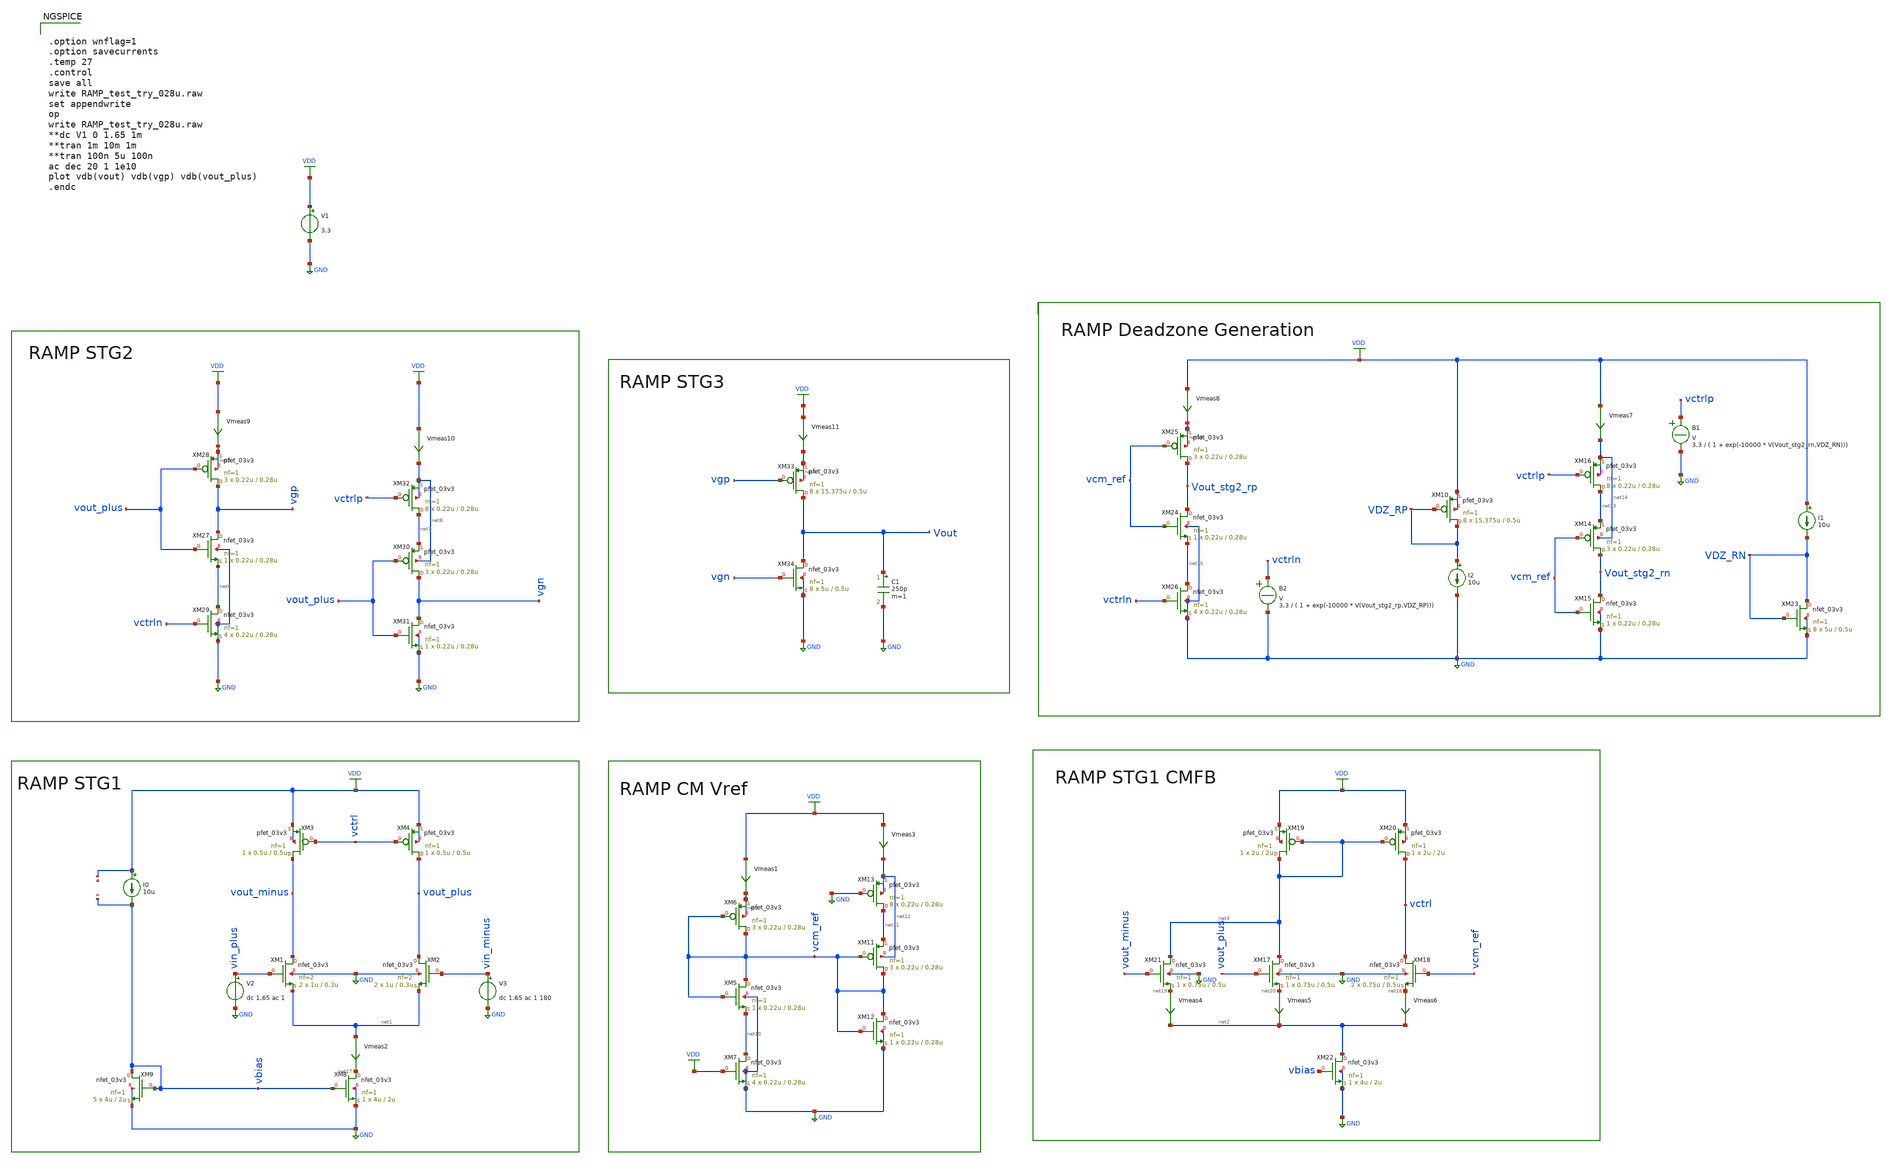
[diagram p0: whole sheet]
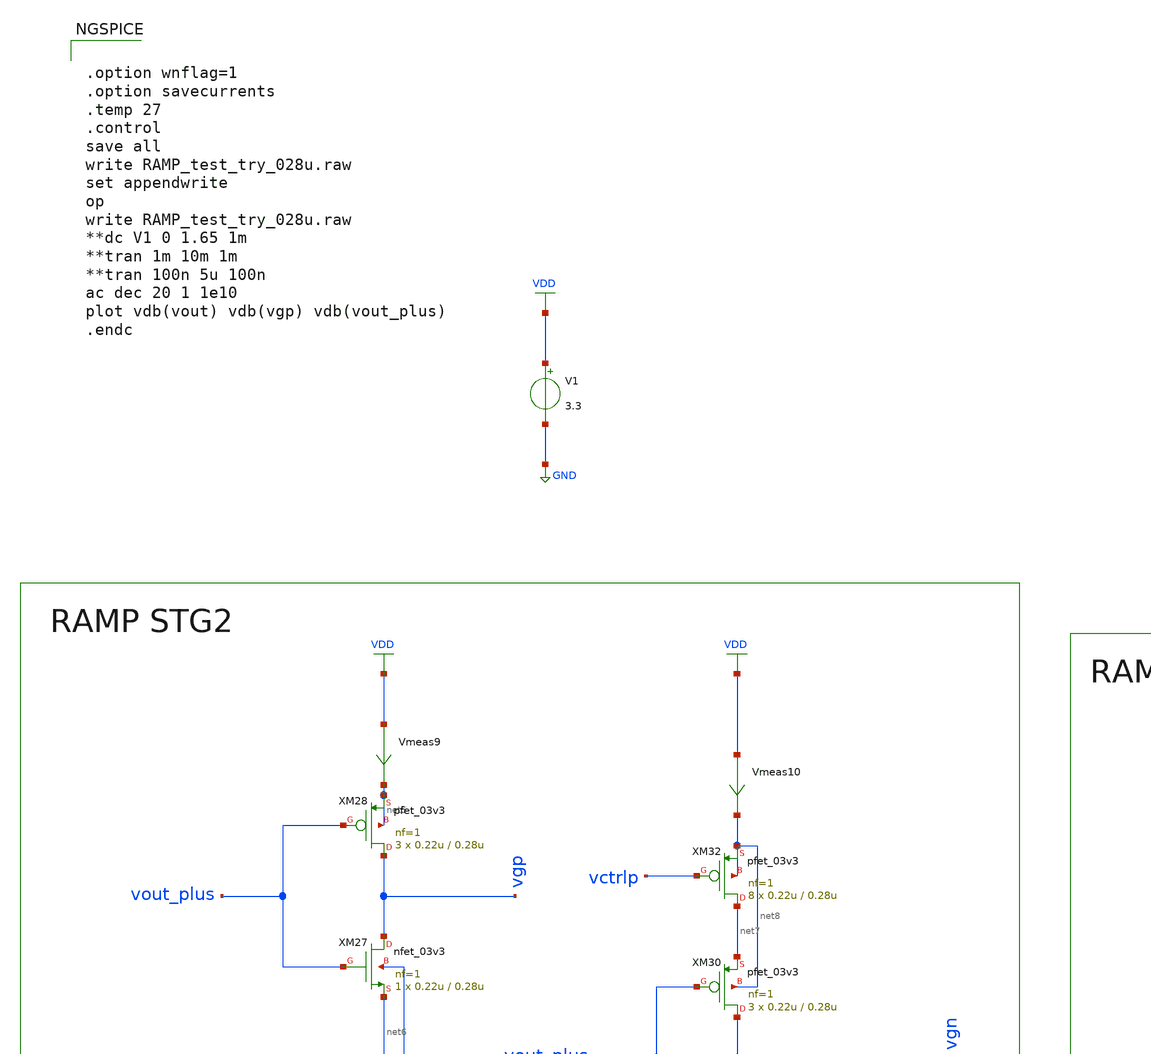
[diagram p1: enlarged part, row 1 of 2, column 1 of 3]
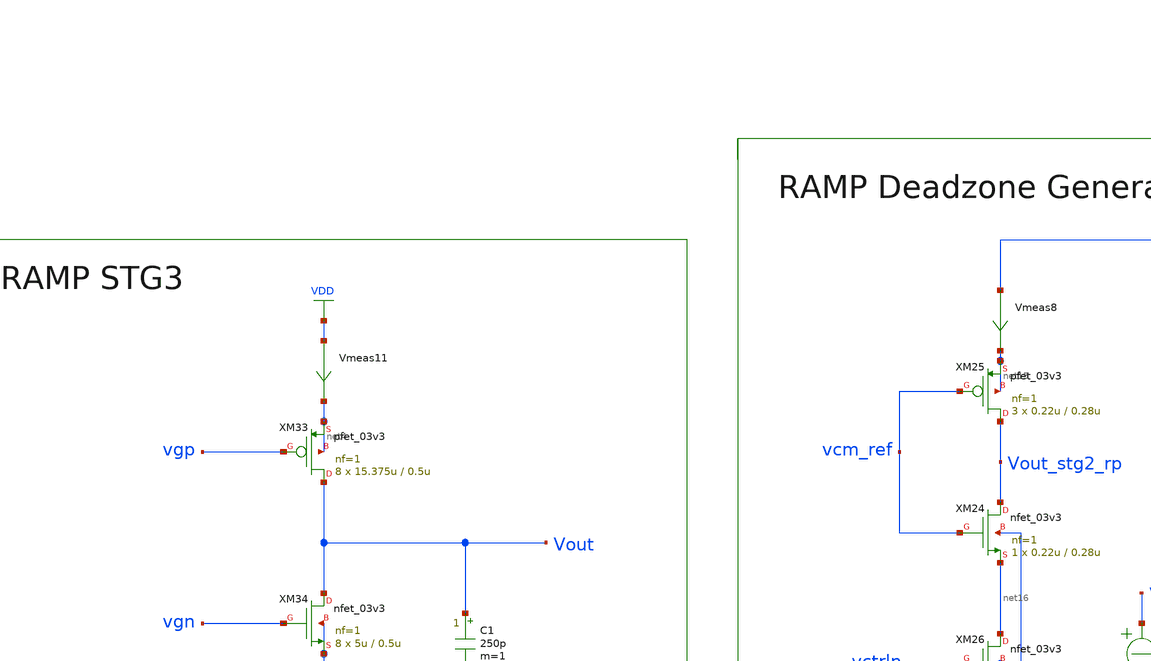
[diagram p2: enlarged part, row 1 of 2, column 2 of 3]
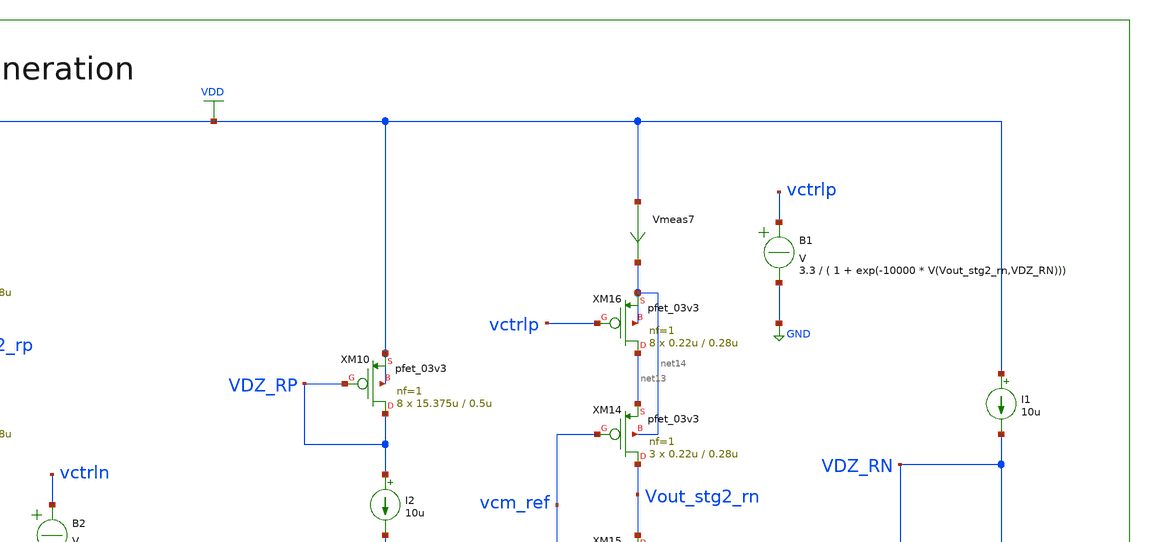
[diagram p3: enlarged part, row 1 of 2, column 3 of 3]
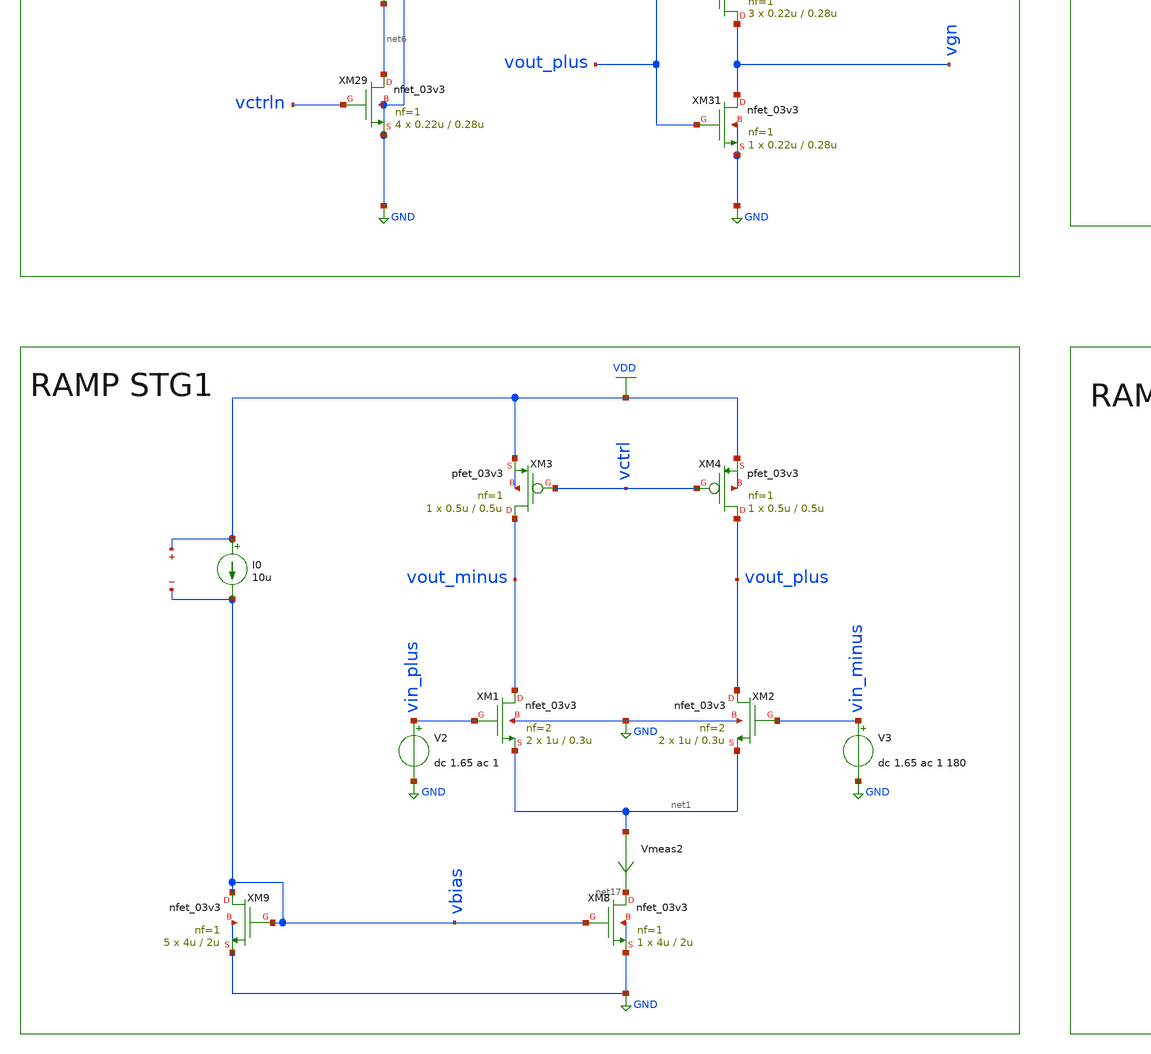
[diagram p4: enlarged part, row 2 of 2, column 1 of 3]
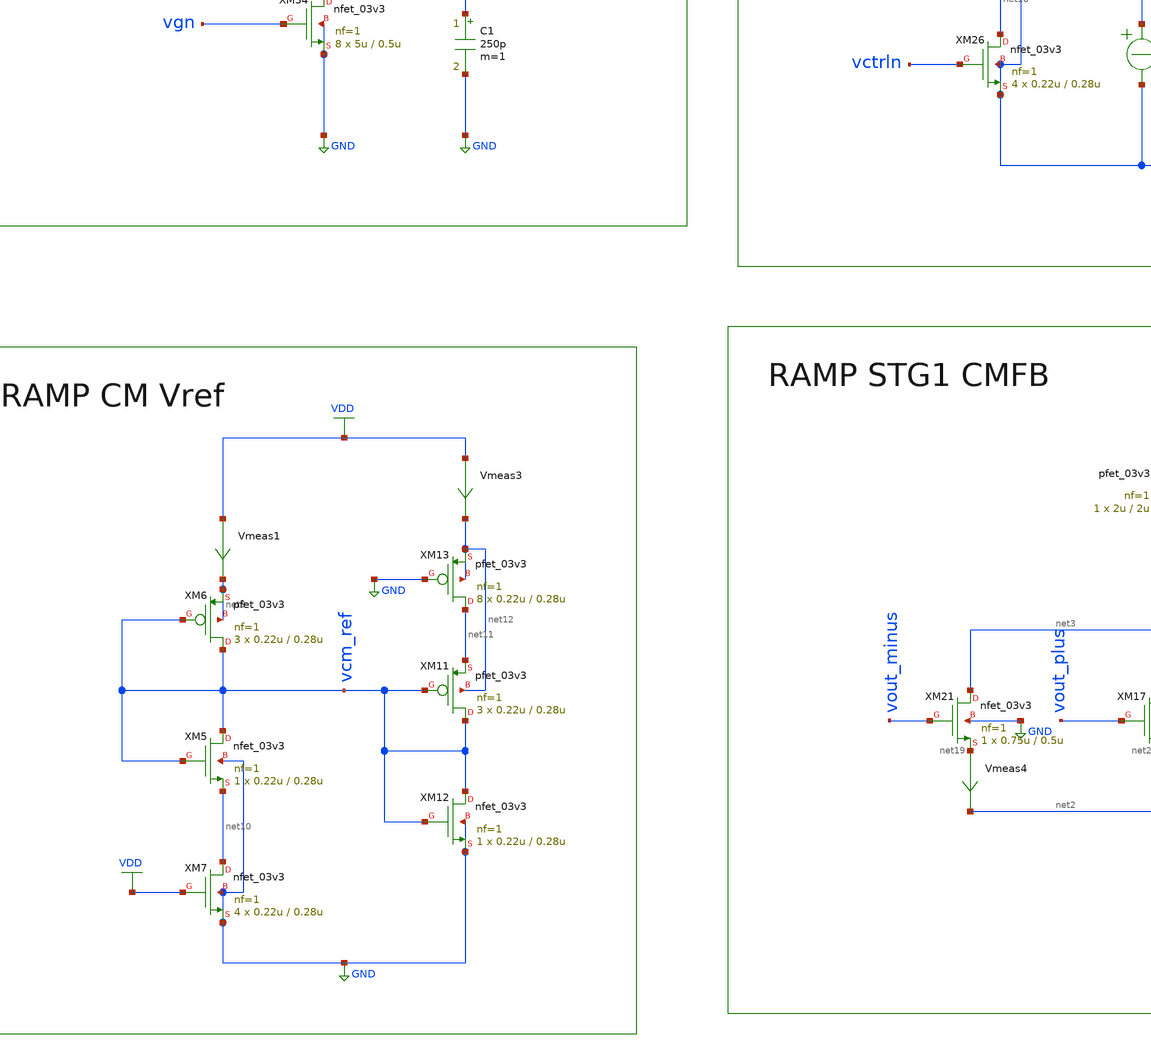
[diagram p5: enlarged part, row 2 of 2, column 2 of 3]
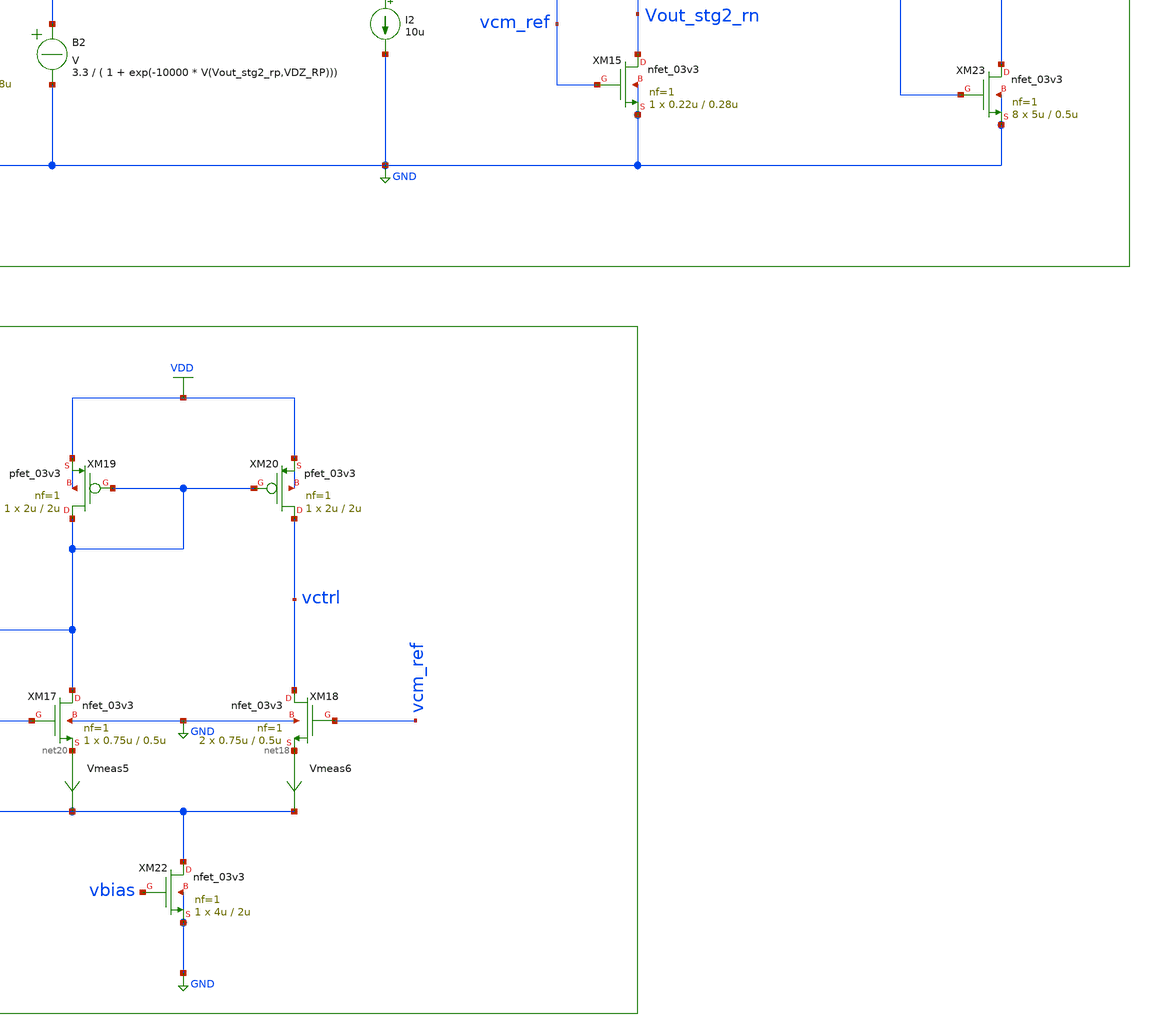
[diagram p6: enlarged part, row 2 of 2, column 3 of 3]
** sch_path: Design_Files/RAMP_test_try_028u.sch
**.subckt RAMP_test_try_028u
XM1 vout_minus vin_plus net1 GND nfet_03v3 L=0.3u W=1u nf=2 ad='int((nf+1)/2) * W/nf * 0.18u' as='int((nf+2)/2) * W/nf * 0.18u'
+ pd='2*int((nf+1)/2) * (W/nf + 0.18u)' ps='2*int((nf+2)/2) * (W/nf + 0.18u)' nrd='0.18u / W' nrs='0.18u / W'
+ sa=0 sb=0 sd=0 m=2
XM3 vout_minus vctrl VDD VDD pfet_03v3 L=0.5u W=0.5u nf=1 ad='int((nf+1)/2) * W/nf * 0.18u' as='int((nf+2)/2) * W/nf * 0.18u'
+ pd='2*int((nf+1)/2) * (W/nf + 0.18u)' ps='2*int((nf+2)/2) * (W/nf + 0.18u)' nrd='0.18u / W' nrs='0.18u / W'
+ sa=0 sb=0 sd=0 m=1
V2 vin_plus GND dc 1.65 ac 1
XM8 net17 vbias GND GND nfet_03v3 L=2u W=4u nf=1 ad='int((nf+1)/2) * W/nf * 0.18u' as='int((nf+2)/2) * W/nf * 0.18u'
+ pd='2*int((nf+1)/2) * (W/nf + 0.18u)' ps='2*int((nf+2)/2) * (W/nf + 0.18u)' nrd='0.18u / W' nrs='0.18u / W'
+ sa=0 sb=0 sd=0 m=1
Vmeas2 net1 net17 0
.save i(vmeas2)
V3 vin_minus GND dc 1.65 ac 1 180
XM9 vbias vbias GND GND nfet_03v3 L=2u W=4u nf=1 ad='int((nf+1)/2) * W/nf * 0.18u' as='int((nf+2)/2) * W/nf * 0.18u'
+ pd='2*int((nf+1)/2) * (W/nf + 0.18u)' ps='2*int((nf+2)/2) * (W/nf + 0.18u)' nrd='0.18u / W' nrs='0.18u / W'
+ sa=0 sb=0 sd=0 m=5
I0 VDD vbias 10u
XM2 vout_plus vin_minus net1 GND nfet_03v3 L=0.3u W=1u nf=2 ad='int((nf+1)/2) * W/nf * 0.18u' as='int((nf+2)/2) * W/nf * 0.18u'
+ pd='2*int((nf+1)/2) * (W/nf + 0.18u)' ps='2*int((nf+2)/2) * (W/nf + 0.18u)' nrd='0.18u / W' nrs='0.18u / W'
+ sa=0 sb=0 sd=0 m=2
XM4 vout_plus vctrl VDD VDD pfet_03v3 L=0.5u W=0.5u nf=1 ad='int((nf+1)/2) * W/nf * 0.18u' as='int((nf+2)/2) * W/nf * 0.18u'
+ pd='2*int((nf+1)/2) * (W/nf + 0.18u)' ps='2*int((nf+2)/2) * (W/nf + 0.18u)' nrd='0.18u / W' nrs='0.18u / W'
+ sa=0 sb=0 sd=0 m=1
V1 VDD GND 3.3
XM18 vctrl vcm_ref net18 GND nfet_03v3 L=0.5u W=0.75u nf=1 ad='int((nf+1)/2) * W/nf * 0.18u' as='int((nf+2)/2) * W/nf * 0.18u'
+ pd='2*int((nf+1)/2) * (W/nf + 0.18u)' ps='2*int((nf+2)/2) * (W/nf + 0.18u)' nrd='0.18u / W' nrs='0.18u / W'
+ sa=0 sb=0 sd=0 m=2
XM19 net3 net3 VDD VDD pfet_03v3 L=2u W=2u nf=1 ad='int((nf+1)/2) * W/nf * 0.18u' as='int((nf+2)/2) * W/nf * 0.18u'
+ pd='2*int((nf+1)/2) * (W/nf + 0.18u)' ps='2*int((nf+2)/2) * (W/nf + 0.18u)' nrd='0.18u / W' nrs='0.18u / W'
+ sa=0 sb=0 sd=0 m=1
XM20 vctrl net3 VDD VDD pfet_03v3 L=2u W=2u nf=1 ad='int((nf+1)/2) * W/nf * 0.18u' as='int((nf+2)/2) * W/nf * 0.18u'
+ pd='2*int((nf+1)/2) * (W/nf + 0.18u)' ps='2*int((nf+2)/2) * (W/nf + 0.18u)' nrd='0.18u / W' nrs='0.18u / W'
+ sa=0 sb=0 sd=0 m=1
XM21 net3 vout_minus net19 GND nfet_03v3 L=0.5u W=0.75u nf=1 ad='int((nf+1)/2) * W/nf * 0.18u' as='int((nf+2)/2) * W/nf * 0.18u'
+ pd='2*int((nf+1)/2) * (W/nf + 0.18u)' ps='2*int((nf+2)/2) * (W/nf + 0.18u)' nrd='0.18u / W' nrs='0.18u / W'
+ sa=0 sb=0 sd=0 m=1
XM22 net2 vbias GND GND nfet_03v3 L=2u W=4u nf=1 ad='int((nf+1)/2) * W/nf * 0.18u' as='int((nf+2)/2) * W/nf * 0.18u'
+ pd='2*int((nf+1)/2) * (W/nf + 0.18u)' ps='2*int((nf+2)/2) * (W/nf + 0.18u)' nrd='0.18u / W' nrs='0.18u / W'
+ sa=0 sb=0 sd=0 m=1
XM17 net3 vout_plus net20 GND nfet_03v3 L=0.5u W=0.75u nf=1 ad='int((nf+1)/2) * W/nf * 0.18u' as='int((nf+2)/2) * W/nf * 0.18u'
+ pd='2*int((nf+1)/2) * (W/nf + 0.18u)' ps='2*int((nf+2)/2) * (W/nf + 0.18u)' nrd='0.18u / W' nrs='0.18u / W'
+ sa=0 sb=0 sd=0 m=1
Vmeas4 net19 net2 0
.save i(vmeas4)
Vmeas5 net20 net2 0
.save i(vmeas5)
Vmeas6 net18 net2 0
.save i(vmeas6)
XM33 Vout vgp net4 net4 pfet_03v3 L=0.5u W=15.375u nf=1 ad='int((nf+1)/2) * W/nf * 0.18u' as='int((nf+2)/2) * W/nf * 0.18u'
+ pd='2*int((nf+1)/2) * (W/nf + 0.18u)' ps='2*int((nf+2)/2) * (W/nf + 0.18u)' nrd='0.18u / W' nrs='0.18u / W'
+ sa=0 sb=0 sd=0 m=8
XM34 Vout vgn GND GND nfet_03v3 L=0.5u W=5u nf=1 ad='int((nf+1)/2) * W/nf * 0.18u' as='int((nf+2)/2) * W/nf * 0.18u'
+ pd='2*int((nf+1)/2) * (W/nf + 0.18u)' ps='2*int((nf+2)/2) * (W/nf + 0.18u)' nrd='0.18u / W' nrs='0.18u / W'
+ sa=0 sb=0 sd=0 m=8
C1 Vout GND 250p m=1
XM27 vgp vout_plus net6 GND nfet_03v3 L=0.28u W=0.22u nf=1 ad='int((nf+1)/2) * W/nf * 0.18u' as='int((nf+2)/2) * W/nf * 0.18u'
+ pd='2*int((nf+1)/2) * (W/nf + 0.18u)' ps='2*int((nf+2)/2) * (W/nf + 0.18u)' nrd='0.18u / W' nrs='0.18u / W'
+ sa=0 sb=0 sd=0 m=1
XM28 vgp vout_plus net5 net5 pfet_03v3 L=0.28u W=0.22u nf=1 ad='int((nf+1)/2) * W/nf * 0.18u' as='int((nf+2)/2) * W/nf * 0.18u'
+ pd='2*int((nf+1)/2) * (W/nf + 0.18u)' ps='2*int((nf+2)/2) * (W/nf + 0.18u)' nrd='0.18u / W' nrs='0.18u / W'
+ sa=0 sb=0 sd=0 m=3
XM29 net6 vctrln GND GND nfet_03v3 L=0.28u W=0.22u nf=1 ad='int((nf+1)/2) * W/nf * 0.18u' as='int((nf+2)/2) * W/nf * 0.18u'
+ pd='2*int((nf+1)/2) * (W/nf + 0.18u)' ps='2*int((nf+2)/2) * (W/nf + 0.18u)' nrd='0.18u / W' nrs='0.18u / W'
+ sa=0 sb=0 sd=0 m=4
Vmeas9 VDD net5 0
.save i(vmeas9)
XM30 vgn vout_plus net7 net8 pfet_03v3 L=0.28u W=0.22u nf=1 ad='int((nf+1)/2) * W/nf * 0.18u' as='int((nf+2)/2) * W/nf * 0.18u'
+ pd='2*int((nf+1)/2) * (W/nf + 0.18u)' ps='2*int((nf+2)/2) * (W/nf + 0.18u)' nrd='0.18u / W' nrs='0.18u / W'
+ sa=0 sb=0 sd=0 m=3
XM31 vgn vout_plus GND GND nfet_03v3 L=0.28u W=0.22u nf=1 ad='int((nf+1)/2) * W/nf * 0.18u' as='int((nf+2)/2) * W/nf * 0.18u'
+ pd='2*int((nf+1)/2) * (W/nf + 0.18u)' ps='2*int((nf+2)/2) * (W/nf + 0.18u)' nrd='0.18u / W' nrs='0.18u / W'
+ sa=0 sb=0 sd=0 m=1
XM32 net7 vctrlp net8 net8 pfet_03v3 L=0.28u W=0.22u nf=1 ad='int((nf+1)/2) * W/nf * 0.18u' as='int((nf+2)/2) * W/nf * 0.18u'
+ pd='2*int((nf+1)/2) * (W/nf + 0.18u)' ps='2*int((nf+2)/2) * (W/nf + 0.18u)' nrd='0.18u / W' nrs='0.18u / W'
+ sa=0 sb=0 sd=0 m=8
Vmeas10 VDD net8 0
.save i(vmeas10)
XM5 vcm_ref vcm_ref net10 GND nfet_03v3 L=0.28u W=0.22u nf=1 ad='int((nf+1)/2) * W/nf * 0.18u' as='int((nf+2)/2) * W/nf * 0.18u'
+ pd='2*int((nf+1)/2) * (W/nf + 0.18u)' ps='2*int((nf+2)/2) * (W/nf + 0.18u)' nrd='0.18u / W' nrs='0.18u / W'
+ sa=0 sb=0 sd=0 m=1
XM6 vcm_ref vcm_ref net9 net9 pfet_03v3 L=0.28u W=0.22u nf=1 ad='int((nf+1)/2) * W/nf * 0.18u' as='int((nf+2)/2) * W/nf * 0.18u'
+ pd='2*int((nf+1)/2) * (W/nf + 0.18u)' ps='2*int((nf+2)/2) * (W/nf + 0.18u)' nrd='0.18u / W' nrs='0.18u / W'
+ sa=0 sb=0 sd=0 m=3
XM7 net10 VDD GND GND nfet_03v3 L=0.28u W=0.22u nf=1 ad='int((nf+1)/2) * W/nf * 0.18u' as='int((nf+2)/2) * W/nf * 0.18u'
+ pd='2*int((nf+1)/2) * (W/nf + 0.18u)' ps='2*int((nf+2)/2) * (W/nf + 0.18u)' nrd='0.18u / W' nrs='0.18u / W'
+ sa=0 sb=0 sd=0 m=4
Vmeas1 VDD net9 0
.save i(vmeas1)
XM11 vcm_ref vcm_ref net11 net12 pfet_03v3 L=0.28u W=0.22u nf=1 ad='int((nf+1)/2) * W/nf * 0.18u' as='int((nf+2)/2) * W/nf * 0.18u'
+ pd='2*int((nf+1)/2) * (W/nf + 0.18u)' ps='2*int((nf+2)/2) * (W/nf + 0.18u)' nrd='0.18u / W' nrs='0.18u / W'
+ sa=0 sb=0 sd=0 m=3
XM12 vcm_ref vcm_ref GND GND nfet_03v3 L=0.28u W=0.22u nf=1 ad='int((nf+1)/2) * W/nf * 0.18u' as='int((nf+2)/2) * W/nf * 0.18u'
+ pd='2*int((nf+1)/2) * (W/nf + 0.18u)' ps='2*int((nf+2)/2) * (W/nf + 0.18u)' nrd='0.18u / W' nrs='0.18u / W'
+ sa=0 sb=0 sd=0 m=1
XM13 net11 GND net12 net12 pfet_03v3 L=0.28u W=0.22u nf=1 ad='int((nf+1)/2) * W/nf * 0.18u' as='int((nf+2)/2) * W/nf * 0.18u'
+ pd='2*int((nf+1)/2) * (W/nf + 0.18u)' ps='2*int((nf+2)/2) * (W/nf + 0.18u)' nrd='0.18u / W' nrs='0.18u / W'
+ sa=0 sb=0 sd=0 m=8
Vmeas3 VDD net12 0
.save i(vmeas3)
XM10 VDZ_RP VDZ_RP VDD VDD pfet_03v3 L=0.5u W=15.375u nf=1 ad='int((nf+1)/2) * W/nf * 0.18u' as='int((nf+2)/2) * W/nf * 0.18u'
+ pd='2*int((nf+1)/2) * (W/nf + 0.18u)' ps='2*int((nf+2)/2) * (W/nf + 0.18u)' nrd='0.18u / W' nrs='0.18u / W'
+ sa=0 sb=0 sd=0 m=8
I2 VDZ_RP GND 10u
B2 vctrln GND V = 3.3 / ( 1 + exp(-10000 * V(Vout_stg2_rp,VDZ_RP)))
XM14 Vout_stg2_rn vcm_ref net13 net14 pfet_03v3 L=0.28u W=0.22u nf=1 ad='int((nf+1)/2) * W/nf * 0.18u'
+ as='int((nf+2)/2) * W/nf * 0.18u' pd='2*int((nf+1)/2) * (W/nf + 0.18u)' ps='2*int((nf+2)/2) * (W/nf + 0.18u)'
+ nrd='0.18u / W' nrs='0.18u / W' sa=0 sb=0 sd=0 m=3
XM15 Vout_stg2_rn vcm_ref GND GND nfet_03v3 L=0.28u W=0.22u nf=1 ad='int((nf+1)/2) * W/nf * 0.18u' as='int((nf+2)/2) * W/nf * 0.18u'
+ pd='2*int((nf+1)/2) * (W/nf + 0.18u)' ps='2*int((nf+2)/2) * (W/nf + 0.18u)' nrd='0.18u / W' nrs='0.18u / W'
+ sa=0 sb=0 sd=0 m=1
XM16 net13 vctrlp net14 net14 pfet_03v3 L=0.28u W=0.22u nf=1 ad='int((nf+1)/2) * W/nf * 0.18u' as='int((nf+2)/2) * W/nf * 0.18u'
+ pd='2*int((nf+1)/2) * (W/nf + 0.18u)' ps='2*int((nf+2)/2) * (W/nf + 0.18u)' nrd='0.18u / W' nrs='0.18u / W'
+ sa=0 sb=0 sd=0 m=8
Vmeas7 VDD net14 0
.save i(vmeas7)
XM23 VDZ_RN VDZ_RN GND GND nfet_03v3 L=0.5u W=5u nf=1 ad='int((nf+1)/2) * W/nf * 0.18u' as='int((nf+2)/2) * W/nf * 0.18u'
+ pd='2*int((nf+1)/2) * (W/nf + 0.18u)' ps='2*int((nf+2)/2) * (W/nf + 0.18u)' nrd='0.18u / W' nrs='0.18u / W'
+ sa=0 sb=0 sd=0 m=8
I1 VDD VDZ_RN 10u
B1 vctrlp GND V = 3.3 / ( 1 + exp(-10000 * V(Vout_stg2_rn,VDZ_RN)))
XM24 Vout_stg2_rp vcm_ref net16 GND nfet_03v3 L=0.28u W=0.22u nf=1 ad='int((nf+1)/2) * W/nf * 0.18u'
+ as='int((nf+2)/2) * W/nf * 0.18u' pd='2*int((nf+1)/2) * (W/nf + 0.18u)' ps='2*int((nf+2)/2) * (W/nf + 0.18u)'
+ nrd='0.18u / W' nrs='0.18u / W' sa=0 sb=0 sd=0 m=1
XM25 Vout_stg2_rp vcm_ref net15 net15 pfet_03v3 L=0.28u W=0.22u nf=1 ad='int((nf+1)/2) * W/nf * 0.18u'
+ as='int((nf+2)/2) * W/nf * 0.18u' pd='2*int((nf+1)/2) * (W/nf + 0.18u)' ps='2*int((nf+2)/2) * (W/nf + 0.18u)'
+ nrd='0.18u / W' nrs='0.18u / W' sa=0 sb=0 sd=0 m=3
XM26 net16 vctrln GND GND nfet_03v3 L=0.28u W=0.22u nf=1 ad='int((nf+1)/2) * W/nf * 0.18u' as='int((nf+2)/2) * W/nf * 0.18u'
+ pd='2*int((nf+1)/2) * (W/nf + 0.18u)' ps='2*int((nf+2)/2) * (W/nf + 0.18u)' nrd='0.18u / W' nrs='0.18u / W'
+ sa=0 sb=0 sd=0 m=4
Vmeas8 VDD net15 0
.save i(vmeas8)
Vmeas11 VDD net4 0
.save i(vmeas11)
.save v(vdd)
.save v(vbias)
**** begin user architecture code


.option wnflag=1
.option savecurrents
.temp 27
.control
save all
write RAMP_test_try_028u.raw
set appendwrite
op
write RAMP_test_try_028u.raw
**dc V1 0 1.65 1m
**tran 1m 10m 1m
**tran 100n 5u 100n
ac dec 20 1 1e10
plot vdb(vout) vdb(vgp) vdb(vout_plus)
.endc




 .save @m.xm1.m0[gm]
.save @m.xm1.m0[id]
.save @m.xm1.m0[vth]
.save @m.xm1.m0[vds]
.save @m.xm1.m0[gds]
.save @m.xm1.m0[cgg]
.save @m.xm1.m0[cgs]
.save @m.xm1.m0[cgd]
.save @m.xm2.m0[gm]
.save @m.xm2.m0[id]
.save @m.xm2.m0[vth]
.save @m.xm2.m0[vds]
.save @m.xm2.m0[gds]
.save @m.xm2.m0[cgg]
.save @m.xm2.m0[cgs]
.save @m.xm2.m0[cgd]
.save @m.xm3.m0[gm]
.save @m.xm3.m0[id]
.save @m.xm3.m0[vth]
.save @m.xm3.m0[vds]
.save @m.xm3.m0[gds]
.save @m.xm3.m0[cgg]
.save @m.xm3.m0[cgs]
.save @m.xm3.m0[cgd]
.save @m.xm4.m0[gm]
.save @m.xm4.m0[id]
.save @m.xm4.m0[vth]
.save @m.xm4.m0[vds]
.save @m.xm4.m0[gds]
.save @m.xm4.m0[cgg]
.save @m.xm4.m0[cgs]
.save @m.xm4.m0[cgd]
.save @m.xm5.m0[gm]
.save @m.xm5.m0[id]
.save @m.xm5.m0[vth]
.save @m.xm5.m0[vds]
.save @m.xm5.m0[gds]
.save @m.xm5.m0[cgg]
.save @m.xm5.m0[cgs]
.save @m.xm5.m0[cgd]
.save @m.xm6.m0[gm]
.save @m.xm6.m0[id]
.save @m.xm6.m0[vth]
.save @m.xm6.m0[vds]
.save @m.xm6.m0[gds]
.save @m.xm6.m0[cgg]
.save @m.xm6.m0[cgs]
.save @m.xm6.m0[cgd]
.save @m.xm7.m0[gm]
.save @m.xm7.m0[id]
.save @m.xm7.m0[vth]
.save @m.xm7.m0[vds]
.save @m.xm7.m0[gds]
.save @m.xm7.m0[cgg]
.save @m.xm7.m0[cgs]
.save @m.xm7.m0[cgd]
.save @m.xm8.m0[gm]
.save @m.xm8.m0[id]
.save @m.xm8.m0[vth]
.save @m.xm8.m0[vds]
.save @m.xm8.m0[gds]
.save @m.xm8.m0[cgg]
.save @m.xm8.m0[cgs]
.save @m.xm8.m0[cgd]
.save @m.xm9.m0[gm]
.save @m.xm9.m0[id]
.save @m.xm9.m0[vth]
.save @m.xm9.m0[vds]
.save @m.xm9.m0[gds]
.save @m.xm9.m0[cgg]
.save @m.xm9.m0[cgs]
.save @m.xm9.m0[cgd]
.save @m.xm10.m0[gm]
.save @m.xm10.m0[id]
.save @m.xm10.m0[vth]
.save @m.xm10.m0[vds]
.save @m.xm10.m0[gds]
.save @m.xm10.m0[cgg]
.save @m.xm10.m0[cgs]
.save @m.xm10.m0[cgd]
.save @m.xm11.m0[gm]
.save @m.xm11.m0[id]
.save @m.xm11.m0[vth]
.save @m.xm11.m0[vds]
.save @m.xm11.m0[gds]
.save @m.xm11.m0[cgg]
.save @m.xm11.m0[cgs]
.save @m.xm11.m0[cgd]
.save @m.xm12.m0[gm]
.save @m.xm12.m0[id]
.save @m.xm12.m0[vth]
.save @m.xm12.m0[vds]
.save @m.xm12.m0[gds]
.save @m.xm12.m0[cgg]
.save @m.xm12.m0[cgs]
.save @m.xm12.m0[cgd]
.save @m.xm13.m0[gm]
.save @m.xm13.m0[id]
.save @m.xm13.m0[vth]
.save @m.xm13.m0[vds]
.save @m.xm13.m0[gds]
.save @m.xm13.m0[cgg]
.save @m.xm13.m0[cgs]
.save @m.xm13.m0[cgd]
.save @m.xm14.m0[gm]
.save @m.xm14.m0[id]
.save @m.xm14.m0[vth]
.save @m.xm14.m0[vds]
.save @m.xm14.m0[gds]
.save @m.xm14.m0[cgg]
.save @m.xm14.m0[cgs]
.save @m.xm14.m0[cgd]
.save @m.xm15.m0[gm]
.save @m.xm15.m0[id]
.save @m.xm15.m0[vth]
.save @m.xm15.m0[vds]
.save @m.xm15.m0[gds]
.save @m.xm15.m0[cgg]
.save @m.xm15.m0[cgs]
.save @m.xm15.m0[cgd]
.save @m.xm16.m0[gm]
.save @m.xm16.m0[id]
.save @m.xm16.m0[vth]
.save @m.xm16.m0[vds]
.save @m.xm16.m0[gds]
.save @m.xm16.m0[cgg]
.save @m.xm16.m0[cgs]
.save @m.xm16.m0[cgd]
.save @m.xm17.m0[gm]
.save @m.xm17.m0[id]
.save @m.xm17.m0[vth]
.save @m.xm17.m0[vds]
.save @m.xm17.m0[gds]
.save @m.xm17.m0[cgg]
.save @m.xm17.m0[cgs]
.save @m.xm17.m0[cgd]
.save @m.xm18.m0[gm]
.save @m.xm18.m0[id]
.save @m.xm18.m0[vth]
.save @m.xm18.m0[vds]
.save @m.xm18.m0[gds]
.save @m.xm18.m0[cgg]
.save @m.xm18.m0[cgs]
.save @m.xm18.m0[cgd]
.save @m.xm19.m0[gm]
.save @m.xm19.m0[id]
.save @m.xm19.m0[vth]
.save @m.xm19.m0[vds]
.save @m.xm19.m0[gds]
.save @m.xm19.m0[cgg]
.save @m.xm19.m0[cgs]
.save @m.xm19.m0[cgd]
.save @m.xm20.m0[gm]
.save @m.xm20.m0[id]
.save @m.xm20.m0[vth]
.save @m.xm20.m0[vds]
.save @m.xm20.m0[gds]
.save @m.xm20.m0[cgg]
.save @m.xm20.m0[cgs]
.save @m.xm20.m0[cgd]
.save @m.xm21.m0[gm]
.save @m.xm21.m0[id]
.save @m.xm21.m0[vth]
.save @m.xm21.m0[vds]
.save @m.xm21.m0[gds]
.save @m.xm21.m0[cgg]
.save @m.xm21.m0[cgs]
.save @m.xm21.m0[cgd]
.save @m.xm22.m0[gm]
.save @m.xm22.m0[id]
.save @m.xm22.m0[vth]
.save @m.xm22.m0[vds]
.save @m.xm22.m0[gds]
.save @m.xm22.m0[cgg]
.save @m.xm22.m0[cgs]
.save @m.xm22.m0[cgd]
.save @m.xm23.m0[gm]
.save @m.xm23.m0[id]
.save @m.xm23.m0[vth]
.save @m.xm23.m0[vds]
.save @m.xm23.m0[gds]
.save @m.xm23.m0[cgg]
.save @m.xm23.m0[cgs]
.save @m.xm23.m0[cgd]
.save @m.xm24.m0[gm]
.save @m.xm24.m0[id]
.save @m.xm24.m0[vth]
.save @m.xm24.m0[vds]
.save @m.xm24.m0[gds]
.save @m.xm24.m0[cgg]
.save @m.xm24.m0[cgs]
.save @m.xm24.m0[cgd]
.save @m.xm25.m0[gm]
.save @m.xm25.m0[id]
.save @m.xm25.m0[vth]
.save @m.xm25.m0[vds]
.save @m.xm25.m0[gds]
.save @m.xm25.m0[cgg]
.save @m.xm25.m0[cgs]
.save @m.xm25.m0[cgd]
.save @m.xm26.m0[gm]
.save @m.xm26.m0[id]
.save @m.xm26.m0[vth]
.save @m.xm26.m0[vds]
.save @m.xm26.m0[gds]
.save @m.xm26.m0[cgg]
.save @m.xm26.m0[cgs]
.save @m.xm26.m0[cgd]
.save @m.xm27.m0[gm]
.save @m.xm27.m0[id]
.save @m.xm27.m0[vth]
.save @m.xm27.m0[vds]
.save @m.xm27.m0[gds]
.save @m.xm27.m0[cgg]
.save @m.xm27.m0[cgs]
.save @m.xm27.m0[cgd]
.save @m.xm28.m0[gm]
.save @m.xm28.m0[id]
.save @m.xm28.m0[vth]
.save @m.xm28.m0[vds]
.save @m.xm28.m0[gds]
.save @m.xm28.m0[cgg]
.save @m.xm28.m0[cgs]
.save @m.xm28.m0[cgd]
.save @m.xm29.m0[gm]
.save @m.xm29.m0[id]
.save @m.xm29.m0[vth]
.save @m.xm29.m0[vds]
.save @m.xm29.m0[gds]
.save @m.xm29.m0[cgg]
.save @m.xm29.m0[cgs]
.save @m.xm29.m0[cgd]
.save @m.xm30.m0[gm]
.save @m.xm30.m0[id]
.save @m.xm30.m0[vth]
.save @m.xm30.m0[vds]
.save @m.xm30.m0[gds]
.save @m.xm30.m0[cgg]
.save @m.xm30.m0[cgs]
.save @m.xm30.m0[cgd]
.save @m.xm31.m0[gm]
.save @m.xm31.m0[id]
.save @m.xm31.m0[vth]
.save @m.xm31.m0[vds]
.save @m.xm31.m0[gds]
.save @m.xm31.m0[cgg]
.save @m.xm31.m0[cgs]
.save @m.xm31.m0[cgd]
.save @m.xm32.m0[gm]
.save @m.xm32.m0[id]
.save @m.xm32.m0[vth]
.save @m.xm32.m0[vds]
.save @m.xm32.m0[gds]
.save @m.xm32.m0[cgg]
.save @m.xm32.m0[cgs]
.save @m.xm32.m0[cgd]
.save @m.xm33.m0[gm]
.save @m.xm33.m0[id]
.save @m.xm33.m0[vth]
.save @m.xm33.m0[vds]
.save @m.xm33.m0[gds]
.save @m.xm33.m0[cgg]
.save @m.xm33.m0[cgs]
.save @m.xm33.m0[cgd]
.save @m.xm34.m0[gm]
.save @m.xm34.m0[id]
.save @m.xm34.m0[vth]
.save @m.xm34.m0[vds]
.save @m.xm34.m0[gds]
.save @m.xm34.m0[cgg]
.save @m.xm34.m0[cgs]
.save @m.xm34.m0[cgd]
.save @m.xm35.m0[gm]
.save @m.xm35.m0[id]
.save @m.xm35.m0[vth]
.save @m.xm35.m0[vds]
.save @m.xm35.m0[gds]
.save @m.xm35.m0[cgg]
.save @m.xm35.m0[cgs]
.save @m.xm35.m0[cgd]
.save @m.xm36.m0[gm]
.save @m.xm36.m0[id]
.save @m.xm36.m0[vth]
.save @m.xm36.m0[vds]
.save @m.xm36.m0[gds]
.save @m.xm36.m0[cgg]
.save @m.xm36.m0[cgs]
.save @m.xm36.m0[cgd]
.save @m.xm37.m0[gm]
.save @m.xm37.m0[id]
.save @m.xm37.m0[vth]
.save @m.xm37.m0[vds]
.save @m.xm37.m0[gds]
.save @m.xm37.m0[cgg]
.save @m.xm37.m0[cgs]
.save @m.xm37.m0[cgd]
.save @m.xm38.m0[gm]
.save @m.xm38.m0[id]
.save @m.xm38.m0[vth]
.save @m.xm38.m0[vds]
.save @m.xm38.m0[gds]
.save @m.xm38.m0[cgg]
.save @m.xm38.m0[cgs]
.save @m.xm38.m0[cgd]
.save @m.xm39.m0[gm]
.save @m.xm39.m0[id]
.save @m.xm39.m0[vth]
.save @m.xm39.m0[vds]
.save @m.xm39.m0[gds]
.save @m.xm39.m0[cgg]
.save @m.xm39.m0[cgs]
.save @m.xm39.m0[cgd]
.save @m.xm40.m0[gm]
.save @m.xm40.m0[id]
.save @m.xm40.m0[vth]
.save @m.xm40.m0[vds]
.save @m.xm40.m0[gds]
.save @m.xm40.m0[cgg]
.save @m.xm40.m0[cgs]
.save @m.xm40.m0[cgd]



.lib /foss/pdks/volare/gf180mcu/versions/0fe599b2afb6708d281543108caf8310912f54af/gf180mcuD/libs.tech/ngspice/sm141064.ngspice typical
.include /foss/pdks/volare/gf180mcu/versions/0fe599b2afb6708d281543108caf8310912f54af/gf180mcuD/libs.tech/ngspice/design.ngspice
.lib /foss/pdks/volare/gf180mcu/versions/0fe599b2afb6708d281543108caf8310912f54af/gf180mcuD/libs.tech/ngspice/sm141064.ngspice res_statistical

**.include $::180MCU_MODELS/design.ngspice
**.lib $::180MCU_MODELS/sm141064.ngspice typical
**.lib $::180MCU_MODELS/sm141064.ngspice res_typical
* .lib $::180MCU_MODELS/sm141064.ngspice res_statistical
*.include $::180MCU_MODELS/design.ngspice
*.lib $::180MCU_MODELS/sm141064.ngspice typical


**** end user architecture code
**.ends
.GLOBAL VDD
.GLOBAL GND
.end
